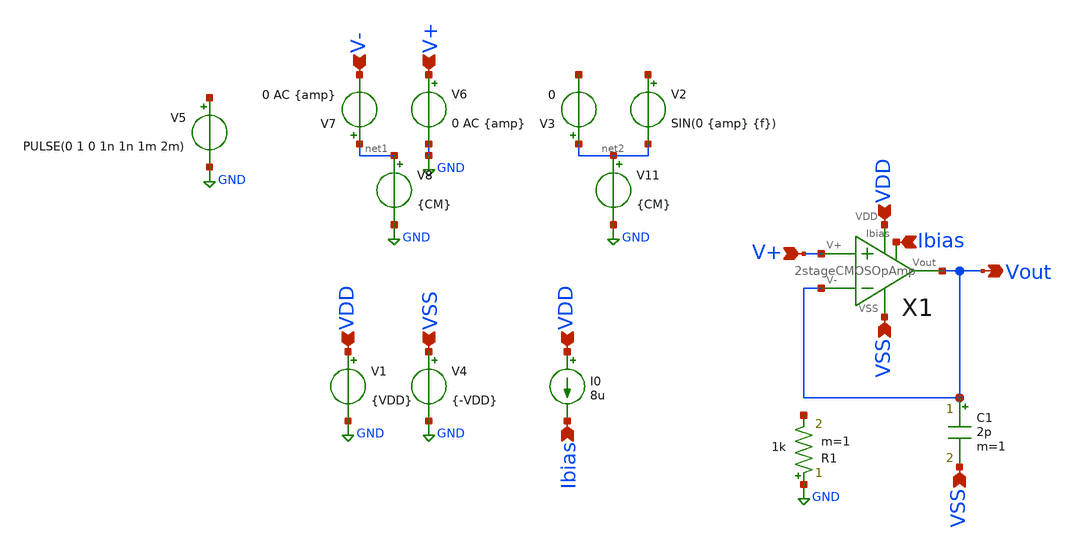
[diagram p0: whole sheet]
** sch_path: ttsky25a-opamp/xschem/2stageCMOSOpAmp_testbed_postlayout.sch
**.subckt 2stageCMOSOpAmp_testbed_postlayout VSS VDD VSS VDD V+ Vout Ibias VDD Ibias VSS V- V+
*.ipin VSS
*.ipin VDD
*.ipin VSS
*.ipin VDD
*.ipin V+
*.opin Vout
*.ipin Ibias
*.ipin VDD
*.ipin Ibias
*.ipin VSS
*.ipin V-
*.ipin V+
V1 VDD GND {VDD}
V4 VSS GND {-VDD}
V6 V+ GND 0 AC {amp}
V7 net1 V- 0 AC {amp}
V8 net1 GND {CM}
V2 net3 net2 SIN(0 {amp} {f})
V3 net2 net4 0
V11 net2 GND {CM}
X1 V+ Vout VSS VDD Vout Ibias 2stageCMOSOpAmp_parax
I0 VDD Ibias 8u
R1 GND net5 1k m=1
V5 net6 GND PULSE(0 1 0 1n 1n 1m 2m)
C1 Vout VSS 2p m=1
**** begin user architecture code



.lib /foss/pdks/sky130A/libs.tech/ngspice/sky130.lib.spice tt
.param CM=0.8 VDD=1.8 amp=1m f=10k
*.tran 1u 10m
.ac dec 20 1 1e12
*.save all

.control
run
*plot vout
plot db(vout/v(v+))
*plot 180*cph(vout)/pi
*set wr_singlescale
*set wr_vecnames
*wrdata /foss/designs/2stageCMOSOpAmp/sim_data_postlayout/GainvsFreq/gain(max).txt db(vout/v(v+))
*wrdata /foss/designs/2stageCMOSOpAmp/sim_data_postlayout/sample_waves/a1.3m_f10k_gain700.txt vout
*wrdata /foss/designs/2stageCMOSOpAmp/sim_data_postlayout/SR/SR.txt vout

.endc


**** end user architecture code
**.ends

* expanding   symbol:  /foss/designs/2stageCMOSOpAmp/ttsky25a-opamp/xschem/2stageCMOSOpAmp_parax.sym
*+ # of pins=6
** sym_path: ttsky25a-opamp/xschem/2stageCMOSOpAmp.sym
.include [file normalize /foss/designs/2stageCMOSOpAmp/ttsky25a-opamp/mag/2stageCMOSOpAmp.sim.spice]
.GLOBAL GND
.end
